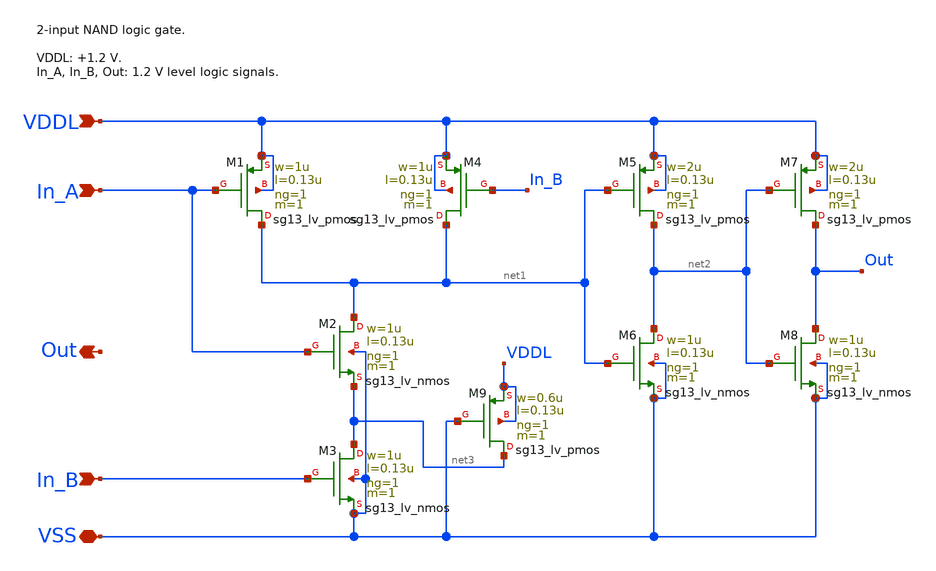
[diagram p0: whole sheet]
** sch_path: sar_adc/xschem/blocks/logic_elements/2-input_NAND/2-input_NAND.sch
**.subckt 2-input_NAND Out VSS VDDL In_A In_B
*.opin Out
*.iopin VSS
*.ipin VDDL
*.ipin In_A
*.ipin In_B
XM1 net1 In_A VDDL VDDL sg13_lv_pmos w=1u l=0.13u ng=1 m=1 mm_ok=1
XM4 net1 In_B VDDL VDDL sg13_lv_pmos w=1u l=0.13u ng=1 m=1 mm_ok=1
XM2 net1 In_A net3 VSS sg13_lv_nmos w=1u l=0.13u ng=1 m=1 mm_ok=1
XM3 net3 In_B VSS VSS sg13_lv_nmos w=1u l=0.13u ng=1 m=1 mm_ok=1
XM5 net2 net1 VDDL VDDL sg13_lv_pmos w=2u l=0.13u ng=1 m=1 mm_ok=1
XM6 net2 net1 VSS VSS sg13_lv_nmos w=1u l=0.13u ng=1 m=1 mm_ok=1
XM7 Out net2 VDDL VDDL sg13_lv_pmos w=2u l=0.13u ng=1 m=1 mm_ok=1
XM8 Out net2 VSS VSS sg13_lv_nmos w=1u l=0.13u ng=1 m=1 mm_ok=1
XM9 net3 VSS VDDL VDDL sg13_lv_pmos w=0.6u l=0.13u ng=1 m=1 mm_ok=1
**.ends
.end
